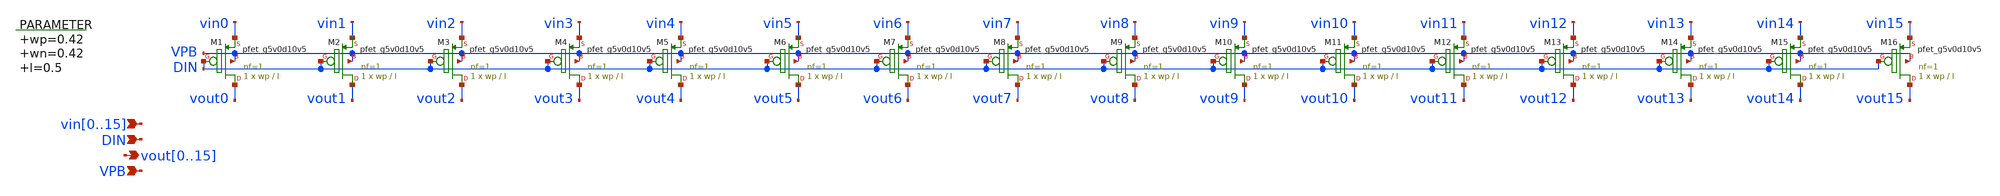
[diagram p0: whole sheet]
** sch_path: xschem/vselector_16b_1v_pmos.sch
**.subckt vselector_16b_1v_pmos
*+ vin0,vin1,vin2,vin3,vin4,vin5,vin6,vin7,vin8,vin9,vin10,vin11,vin12,vin13,vin14,vin15
*+ vout0,vout1,vout2,vout3,vout4,vout5,vout6,vout7,vout8,vout9,vout10,vout11,vout12,vout13,vout14,vout15 VPB DIN
*.ipin vin0,vin1,vin2,vin3,vin4,vin5,vin6,vin7,vin8,vin9,vin10,vin11,vin12,vin13,vin14,vin15
*.opin
*+ vout0,vout1,vout2,vout3,vout4,vout5,vout6,vout7,vout8,vout9,vout10,vout11,vout12,vout13,vout14,vout15
*.ipin VPB
*.ipin DIN
.param wp=0.42 wn=0.42 l=0.5

XM1 vout0 DIN vin0 VPB sky130_fd_pr__pfet_g5v0d10v5 L=l W=wp nf=1 ad='int((nf+1)/2) * W/nf * 0.29' as='int((nf+2)/2) * W/nf * 0.29'
+ pd='2*int((nf+1)/2) * (W/nf + 0.29)' ps='2*int((nf+2)/2) * (W/nf + 0.29)' nrd='0.29 / W' nrs='0.29 / W'
+ sa=0 sb=0 sd=0 mult=1 m=1
XM2 vout1 DIN vin1 VPB sky130_fd_pr__pfet_g5v0d10v5 L=l W=wp nf=1 ad='int((nf+1)/2) * W/nf * 0.29' as='int((nf+2)/2) * W/nf * 0.29'
+ pd='2*int((nf+1)/2) * (W/nf + 0.29)' ps='2*int((nf+2)/2) * (W/nf + 0.29)' nrd='0.29 / W' nrs='0.29 / W'
+ sa=0 sb=0 sd=0 mult=1 m=1
XM3 vout2 DIN vin2 VPB sky130_fd_pr__pfet_g5v0d10v5 L=l W=wp nf=1 ad='int((nf+1)/2) * W/nf * 0.29' as='int((nf+2)/2) * W/nf * 0.29'
+ pd='2*int((nf+1)/2) * (W/nf + 0.29)' ps='2*int((nf+2)/2) * (W/nf + 0.29)' nrd='0.29 / W' nrs='0.29 / W'
+ sa=0 sb=0 sd=0 mult=1 m=1
XM4 vout3 DIN vin3 VPB sky130_fd_pr__pfet_g5v0d10v5 L=l W=wp nf=1 ad='int((nf+1)/2) * W/nf * 0.29' as='int((nf+2)/2) * W/nf * 0.29'
+ pd='2*int((nf+1)/2) * (W/nf + 0.29)' ps='2*int((nf+2)/2) * (W/nf + 0.29)' nrd='0.29 / W' nrs='0.29 / W'
+ sa=0 sb=0 sd=0 mult=1 m=1
XM5 vout4 DIN vin4 VPB sky130_fd_pr__pfet_g5v0d10v5 L=l W=wp nf=1 ad='int((nf+1)/2) * W/nf * 0.29' as='int((nf+2)/2) * W/nf * 0.29'
+ pd='2*int((nf+1)/2) * (W/nf + 0.29)' ps='2*int((nf+2)/2) * (W/nf + 0.29)' nrd='0.29 / W' nrs='0.29 / W'
+ sa=0 sb=0 sd=0 mult=1 m=1
XM6 vout5 DIN vin5 VPB sky130_fd_pr__pfet_g5v0d10v5 L=l W=wp nf=1 ad='int((nf+1)/2) * W/nf * 0.29' as='int((nf+2)/2) * W/nf * 0.29'
+ pd='2*int((nf+1)/2) * (W/nf + 0.29)' ps='2*int((nf+2)/2) * (W/nf + 0.29)' nrd='0.29 / W' nrs='0.29 / W'
+ sa=0 sb=0 sd=0 mult=1 m=1
XM7 vout6 DIN vin6 VPB sky130_fd_pr__pfet_g5v0d10v5 L=l W=wp nf=1 ad='int((nf+1)/2) * W/nf * 0.29' as='int((nf+2)/2) * W/nf * 0.29'
+ pd='2*int((nf+1)/2) * (W/nf + 0.29)' ps='2*int((nf+2)/2) * (W/nf + 0.29)' nrd='0.29 / W' nrs='0.29 / W'
+ sa=0 sb=0 sd=0 mult=1 m=1
XM8 vout7 DIN vin7 VPB sky130_fd_pr__pfet_g5v0d10v5 L=l W=wp nf=1 ad='int((nf+1)/2) * W/nf * 0.29' as='int((nf+2)/2) * W/nf * 0.29'
+ pd='2*int((nf+1)/2) * (W/nf + 0.29)' ps='2*int((nf+2)/2) * (W/nf + 0.29)' nrd='0.29 / W' nrs='0.29 / W'
+ sa=0 sb=0 sd=0 mult=1 m=1
XM9 vout8 DIN vin8 VPB sky130_fd_pr__pfet_g5v0d10v5 L=l W=wp nf=1 ad='int((nf+1)/2) * W/nf * 0.29' as='int((nf+2)/2) * W/nf * 0.29'
+ pd='2*int((nf+1)/2) * (W/nf + 0.29)' ps='2*int((nf+2)/2) * (W/nf + 0.29)' nrd='0.29 / W' nrs='0.29 / W'
+ sa=0 sb=0 sd=0 mult=1 m=1
XM10 vout9 DIN vin9 VPB sky130_fd_pr__pfet_g5v0d10v5 L=l W=wp nf=1 ad='int((nf+1)/2) * W/nf * 0.29' as='int((nf+2)/2) * W/nf * 0.29'
+ pd='2*int((nf+1)/2) * (W/nf + 0.29)' ps='2*int((nf+2)/2) * (W/nf + 0.29)' nrd='0.29 / W' nrs='0.29 / W'
+ sa=0 sb=0 sd=0 mult=1 m=1
XM11 vout10 DIN vin10 VPB sky130_fd_pr__pfet_g5v0d10v5 L=l W=wp nf=1 ad='int((nf+1)/2) * W/nf * 0.29'
+ as='int((nf+2)/2) * W/nf * 0.29' pd='2*int((nf+1)/2) * (W/nf + 0.29)' ps='2*int((nf+2)/2) * (W/nf + 0.29)'
+ nrd='0.29 / W' nrs='0.29 / W' sa=0 sb=0 sd=0 mult=1 m=1
XM12 vout11 DIN vin11 VPB sky130_fd_pr__pfet_g5v0d10v5 L=l W=wp nf=1 ad='int((nf+1)/2) * W/nf * 0.29'
+ as='int((nf+2)/2) * W/nf * 0.29' pd='2*int((nf+1)/2) * (W/nf + 0.29)' ps='2*int((nf+2)/2) * (W/nf + 0.29)'
+ nrd='0.29 / W' nrs='0.29 / W' sa=0 sb=0 sd=0 mult=1 m=1
XM13 vout12 DIN vin12 VPB sky130_fd_pr__pfet_g5v0d10v5 L=l W=wp nf=1 ad='int((nf+1)/2) * W/nf * 0.29'
+ as='int((nf+2)/2) * W/nf * 0.29' pd='2*int((nf+1)/2) * (W/nf + 0.29)' ps='2*int((nf+2)/2) * (W/nf + 0.29)'
+ nrd='0.29 / W' nrs='0.29 / W' sa=0 sb=0 sd=0 mult=1 m=1
XM14 vout13 DIN vin13 VPB sky130_fd_pr__pfet_g5v0d10v5 L=l W=wp nf=1 ad='int((nf+1)/2) * W/nf * 0.29'
+ as='int((nf+2)/2) * W/nf * 0.29' pd='2*int((nf+1)/2) * (W/nf + 0.29)' ps='2*int((nf+2)/2) * (W/nf + 0.29)'
+ nrd='0.29 / W' nrs='0.29 / W' sa=0 sb=0 sd=0 mult=1 m=1
XM15 vout14 DIN vin14 VPB sky130_fd_pr__pfet_g5v0d10v5 L=l W=wp nf=1 ad='int((nf+1)/2) * W/nf * 0.29'
+ as='int((nf+2)/2) * W/nf * 0.29' pd='2*int((nf+1)/2) * (W/nf + 0.29)' ps='2*int((nf+2)/2) * (W/nf + 0.29)'
+ nrd='0.29 / W' nrs='0.29 / W' sa=0 sb=0 sd=0 mult=1 m=1
XM16 vout15 DIN vin15 VPB sky130_fd_pr__pfet_g5v0d10v5 L=l W=wp nf=1 ad='int((nf+1)/2) * W/nf * 0.29'
+ as='int((nf+2)/2) * W/nf * 0.29' pd='2*int((nf+1)/2) * (W/nf + 0.29)' ps='2*int((nf+2)/2) * (W/nf + 0.29)'
+ nrd='0.29 / W' nrs='0.29 / W' sa=0 sb=0 sd=0 mult=1 m=1
**.ends
.end
